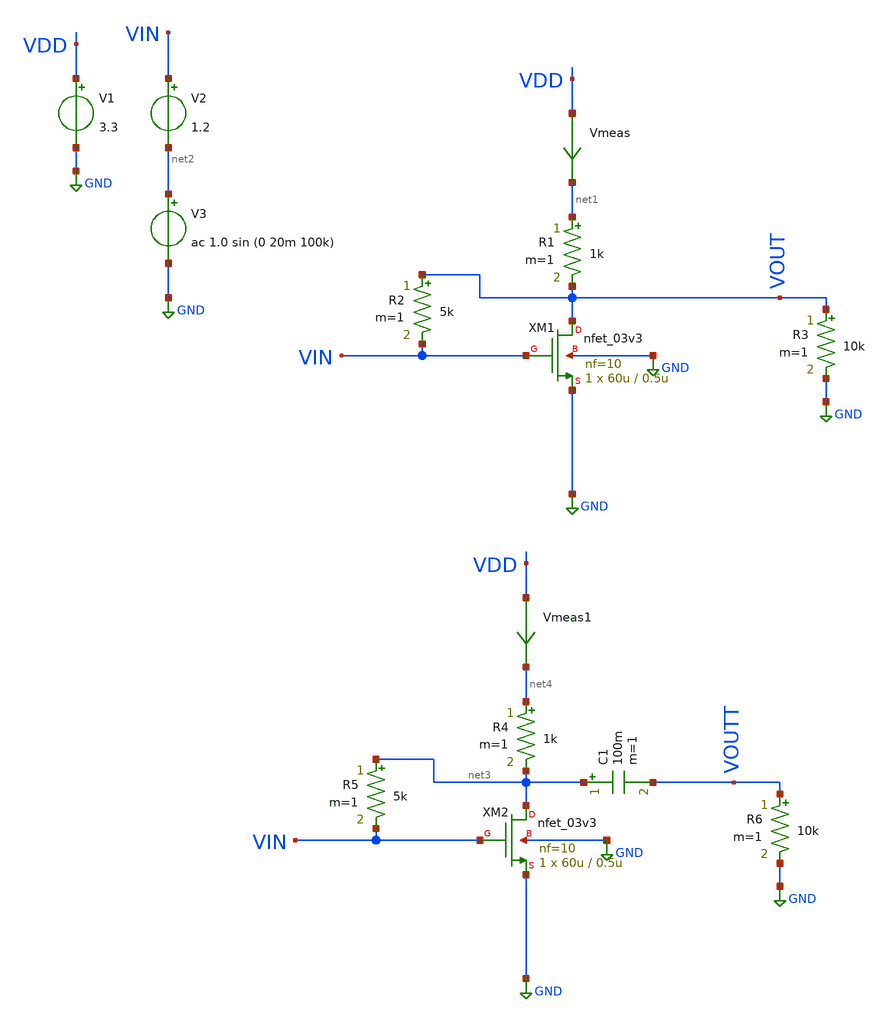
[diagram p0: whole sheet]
** sch_path: gain_with_load/simple_amp_with_load1.sch
**.subckt simple_amp_with_load1
XM1 VOUT VIN GND GND nfet_03v3 L=0.5u W=60u nf=10 ad='int((nf+1)/2) * W/nf * 0.18u' as='int((nf+2)/2) * W/nf * 0.18u'
+ pd='2*int((nf+1)/2) * (W/nf + 0.18u)' ps='2*int((nf+2)/2) * (W/nf + 0.18u)' nrd='0.18u / W' nrs='0.18u / W'
+ sa=0 sb=0 sd=0 m=1
Vmeas VDD net1 0
.save i(vmeas)
V1 VDD GND 3.3
V2 VIN net2 1.2
V3 net2 GND ac 1.0 sin (0 20m 100k)
R1 net1 VOUT 1k m=1
R2 VOUT VIN 5k m=1
R3 VOUT GND 10k m=1
XM2 net3 VIN GND GND nfet_03v3 L=0.5u W=60u nf=10 ad='int((nf+1)/2) * W/nf * 0.18u' as='int((nf+2)/2) * W/nf * 0.18u'
+ pd='2*int((nf+1)/2) * (W/nf + 0.18u)' ps='2*int((nf+2)/2) * (W/nf + 0.18u)' nrd='0.18u / W' nrs='0.18u / W'
+ sa=0 sb=0 sd=0 m=1
Vmeas1 VDD net4 0
.save i(vmeas1)
R4 net4 net3 1k m=1
R5 net3 VIN 5k m=1
R6 VOUTT GND 10k m=1
C1 net3 VOUTT 100m m=1
**** begin user architecture code

.include $::180MCU_MODELS/design.ngspice
*.lib $::180MCU_MODELS/sm141064.ngspice statistical
*.lib $::180MCU_MODELS/sm141064.ngspice res_statistical
.lib $::180MCU_MODELS/sm141064.ngspice typical
.lib $::180MCU_MODELS/sm141064.ngspice res_typical
.lib $::180MCU_MODELS/sm141064.ngspice moscap_typical
.lib $::180MCU_MODELS/sm141064.ngspice bjt_typical
.lib $::180MCU_MODELS/sm141064.ngspice diode_typical
.lib $::180MCU_MODELS/sm141064.ngspice mimcap_typical
.TEMP 27

.param   sw_stat_global = 1   sw_stat_mism = 1  mc_skew = 3  res_mc_skew = 3  cap_mc_skew = 3
+  fnoicor = 1



.control
save all
dc V2 0 3.3 0.01


plot v(VOUT) deriv(v(VOUT)) v(VIN)
plot v(VOUT) deriv(v(VOUT))
plot i(Vmeas)
plot deriv(v(VOUT))
tran 10ns 20u
plot (v(VOUTT)) (v(VIN)-1.2)
plot fft((v(VOUTT))) fft((v(VIN)))
ac dec 20 1 50G
plot v(VOUT)
.endc

**** end user architecture code
**.ends
.GLOBAL GND
.end
